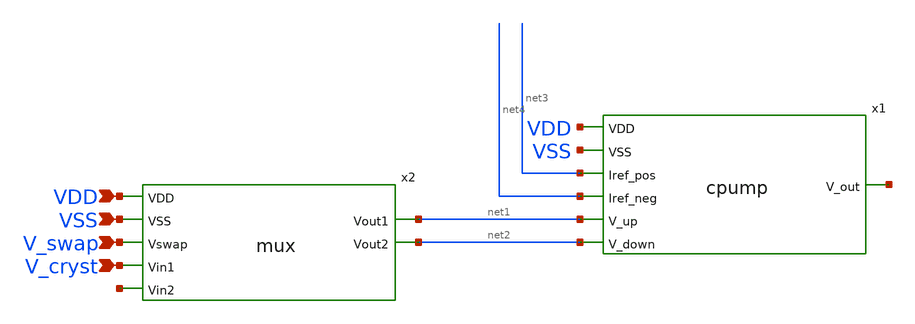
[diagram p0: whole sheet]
** sch_path: blocks/pll/pll.sch
**.subckt pll VDD VSS V_swap V_cryst
*.ipin VDD
*.ipin VSS
*.ipin V_swap
*.ipin V_cryst
x1 net3 VDD net1 net5 net2 VSS net4 cpump
x2 net2 net6 VDD V_swap VSS net1 V_cryst mux
**.ends

* expanding   symbol:  blocks/pll/cpump.sym # of pins=7
** sym_path: blocks/pll/cpump.sym
** sch_path: blocks/pll/cpump.sch
.subckt cpump Iref_pos VDD V_up V_out V_down VSS Iref_neg
*.ipin Iref_pos
*.ipin Iref_neg
*.ipin V_up
*.ipin V_down
*.ipin VDD
*.ipin VSS
*.opin V_out
XM1 V_out V_up Iref_pos VDD pfet_03v3 L=1u W=40u nf=10 ad='int((nf+1)/2) * W/nf * 0.18u' as='int((nf+2)/2) * W/nf * 0.18u'
+ pd='2*int((nf+1)/2) * (W/nf + 0.18u)' ps='2*int((nf+2)/2) * (W/nf + 0.18u)' nrd='0.18u / W' nrs='0.18u / W'
+ sa=0 sb=0 sd=0 m=1
XM2 V_out V_down Iref_neg VSS nfet_03v3 L=1u W=4u nf=1 ad='int((nf+1)/2) * W/nf * 0.18u' as='int((nf+2)/2) * W/nf * 0.18u'
+ pd='2*int((nf+1)/2) * (W/nf + 0.18u)' ps='2*int((nf+2)/2) * (W/nf + 0.18u)' nrd='0.18u / W' nrs='0.18u / W'
+ sa=0 sb=0 sd=0 m=1
XR1 net1 V_out VSS ppolyf_u r_width=2e-6 r_length=8e-6 m=1
XC1 net1 VSS cap_mim_2f0_m4m5_noshield c_width=5e-6 c_length=5e-6 m=1
XC2 V_out VSS cap_mim_2f0_m4m5_noshield c_width=5e-6 c_length=5e-6 m=1
.ends


* expanding   symbol:  blocks/pll/mux.sym # of pins=7
** sym_path: blocks/pll/mux.sym
** sch_path: blocks/pll/mux.sch
.subckt mux Vout2 Vin2 VDD Vswap VSS Vout1 Vin1
*.ipin Vin1
*.opin Vout1
*.ipin Vin2
*.opin Vout2
*.ipin VDD
*.ipin VSS
*.ipin Vswap
XM1 Vout1 net1 Vin1 net3 nfet_03v3 L=1u W=4u nf=1 ad='int((nf+1)/2) * W/nf * 0.18u' as='int((nf+2)/2) * W/nf * 0.18u'
+ pd='2*int((nf+1)/2) * (W/nf + 0.18u)' ps='2*int((nf+2)/2) * (W/nf + 0.18u)' nrd='0.18u / W' nrs='0.18u / W'
+ sa=0 sb=0 sd=0 m=1
XM2 Vout1 Vswap Vin1 net4 pfet_03v3 L=1u W=16u nf=4 ad='int((nf+1)/2) * W/nf * 0.18u' as='int((nf+2)/2) * W/nf * 0.18u'
+ pd='2*int((nf+1)/2) * (W/nf + 0.18u)' ps='2*int((nf+2)/2) * (W/nf + 0.18u)' nrd='0.18u / W' nrs='0.18u / W'
+ sa=0 sb=0 sd=0 m=1
XM3 Vout2 Vswap Vin2 net5 nfet_03v3 L=1u W=4u nf=1 ad='int((nf+1)/2) * W/nf * 0.18u' as='int((nf+2)/2) * W/nf * 0.18u'
+ pd='2*int((nf+1)/2) * (W/nf + 0.18u)' ps='2*int((nf+2)/2) * (W/nf + 0.18u)' nrd='0.18u / W' nrs='0.18u / W'
+ sa=0 sb=0 sd=0 m=1
XM4 Vout2 net1 Vin2 net6 pfet_03v3 L=1u W=16u nf=4 ad='int((nf+1)/2) * W/nf * 0.18u' as='int((nf+2)/2) * W/nf * 0.18u'
+ pd='2*int((nf+1)/2) * (W/nf + 0.18u)' ps='2*int((nf+2)/2) * (W/nf + 0.18u)' nrd='0.18u / W' nrs='0.18u / W'
+ sa=0 sb=0 sd=0 m=1
XM5 Vswap net1 VSS VSS nfet_03v3 L=1u W=1u nf=1 ad='int((nf+1)/2) * W/nf * 0.18u' as='int((nf+2)/2) * W/nf * 0.18u'
+ pd='2*int((nf+1)/2) * (W/nf + 0.18u)' ps='2*int((nf+2)/2) * (W/nf + 0.18u)' nrd='0.18u / W' nrs='0.18u / W'
+ sa=0 sb=0 sd=0 m=1
XM6 VDD net1 Vswap net2 pfet_03v3 L=1u W=4u nf=4 ad='int((nf+1)/2) * W/nf * 0.18u' as='int((nf+2)/2) * W/nf * 0.18u'
+ pd='2*int((nf+1)/2) * (W/nf + 0.18u)' ps='2*int((nf+2)/2) * (W/nf + 0.18u)' nrd='0.18u / W' nrs='0.18u / W'
+ sa=0 sb=0 sd=0 m=1
.ends

.end
